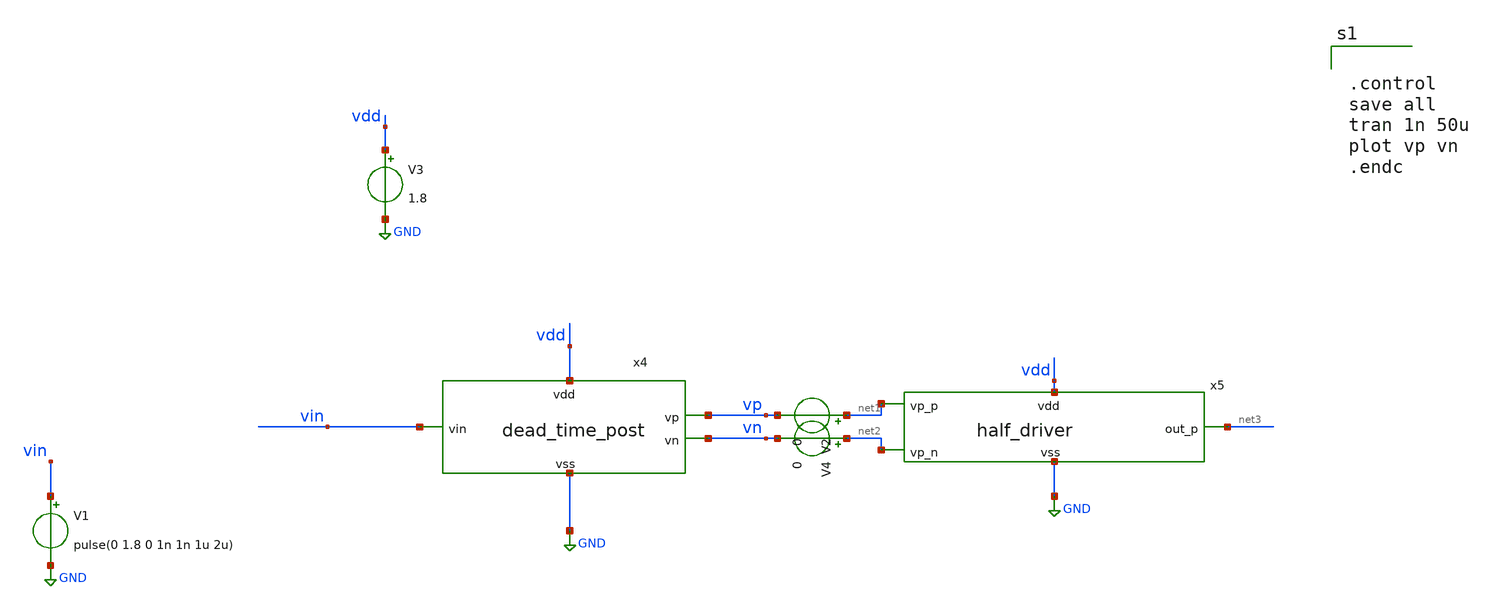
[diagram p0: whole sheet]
** sch_path: xschem/src/dead_time/dead_time_tb.sch
**.subckt dead_time_tb
V1 vin GND pulse(0 1.8 0 1n 1n 1u 2u)
V3 vdd GND 1.8
x4 vdd vin vp vn GND dead_time_post
x5 vdd GND net1 net3 net2 half_driver
V2 net1 vp 0
V4 net2 vn 0
**** begin user architecture code

.include /home/eda/pdk/skywater-pdk/libraries/sky130_fd_pr_ngspice/latest/models/corners/tt.spice
.include /home/eda/magic/class_d_audio_amplifier/dead_time/dead_time_post.spice

* Resistor$::SKYWATER_MODELS/Capacitor
.include $::SKYWATER_MODELS/models/r+c/res_typical__cap_typical.spice
.include $::SKYWATER_MODELS/models/r+c/res_typical__cap_typical__lin.spice
* Special cells
.include $::SKYWATER_MODELS/models/corners/tt/specialized_cells.spice




.control
save all
tran 1n 50u
plot vp vn
.endc



**** end user architecture code
**.ends

* expanding   symbol:  src/output_driver/half_driver.sym # of pins=5
** sym_path: xschem/src/output_driver/half_driver.sym
** sch_path: xschem/src/output_driver/half_driver.sch
.subckt half_driver vdd vss vp_p out_p vp_n
*.ipin vp_p
*.ipin vp_n
*.opin out_p
*.iopin vdd
*.iopin vss
XM1 out_p vp_p vdd vdd sky130_fd_pr__pfet_01v8 L=0.15 W=12000 nf=200 ad='int((nf+1)/2) * W/nf * 0.29'
+ as='int((nf+2)/2) * W/nf * 0.29' pd='2*int((nf+1)/2) * (W/nf + 0.29)' ps='2*int((nf+2)/2) * (W/nf + 0.29)'
+ nrd='0.29 / W' nrs='0.29 / W' sa=0 sb=0 sd=0 mult=1 m=1
XM2 out_p vp_n vss vss sky130_fd_pr__nfet_01v8 L=0.15 W=2400 nf=100 ad='int((nf+1)/2) * W/nf * 0.29'
+ as='int((nf+2)/2) * W/nf * 0.29' pd='2*int((nf+1)/2) * (W/nf + 0.29)' ps='2*int((nf+2)/2) * (W/nf + 0.29)'
+ nrd='0.29 / W' nrs='0.29 / W' sa=0 sb=0 sd=0 mult=1 m=1
.ends

.GLOBAL GND
.end
